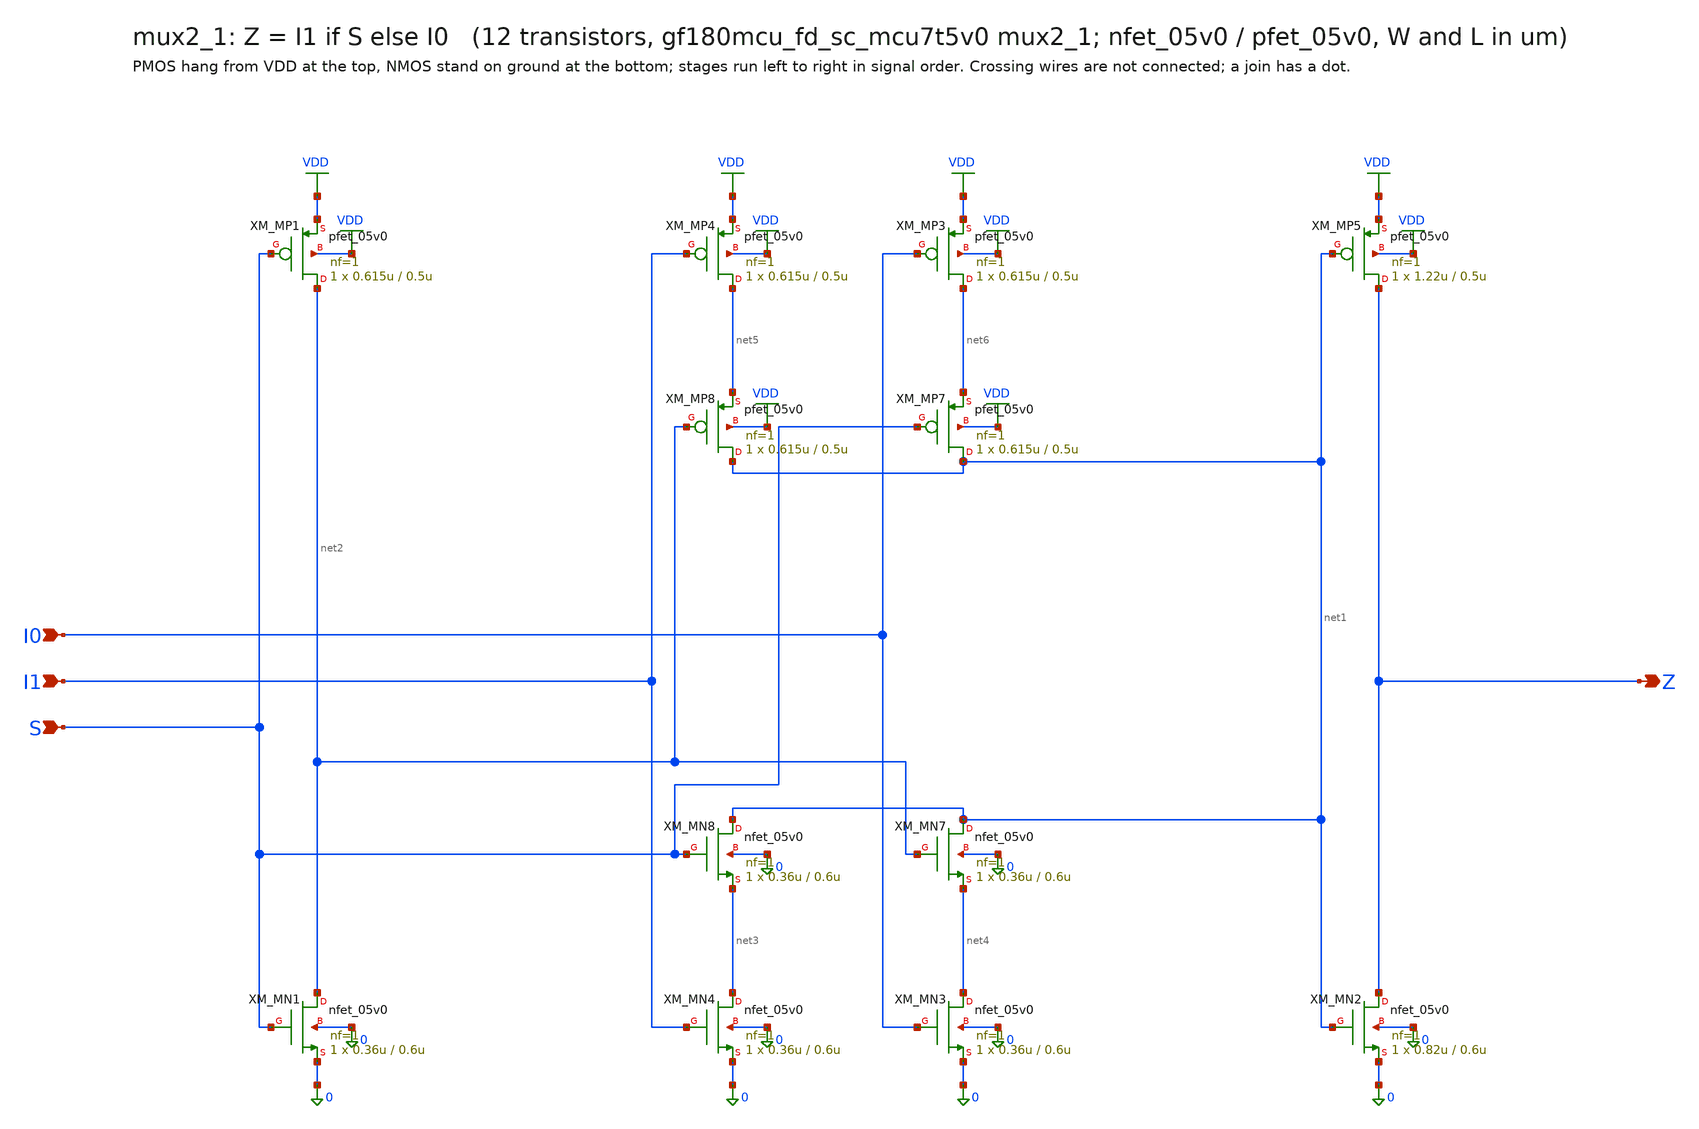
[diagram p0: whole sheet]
** sch_path: xschem/cells_tx/mux2_1.sch
**.subckt mux2_1 I0 I1 S Z
*.ipin I0
*.ipin I1
*.ipin S
*.opin Z
XM_MN2 Z net1 0 0 nfet_05v0 L=0.6u W=0.82u nf=1 ad=4.1e-13 as=4.1e-13 pd=2.64e-06 ps=2.64e-06 nrd=0
+ nrs=0 sa=0 sb=0 sd=0 m=1
XM_MN4 net3 I1 0 0 nfet_05v0 L=0.6u W=0.36u nf=1 ad=1.8e-13 as=1.8e-13 pd=1.72e-06 ps=1.72e-06 nrd=0
+ nrs=0 sa=0 sb=0 sd=0 m=1
XM_MN8 net1 S net3 0 nfet_05v0 L=0.6u W=0.36u nf=1 ad=1.8e-13 as=1.8e-13 pd=1.72e-06 ps=1.72e-06
+ nrd=0 nrs=0 sa=0 sb=0 sd=0 m=1
XM_MN7 net1 net2 net4 0 nfet_05v0 L=0.6u W=0.36u nf=1 ad=1.8e-13 as=1.8e-13 pd=1.72e-06 ps=1.72e-06
+ nrd=0 nrs=0 sa=0 sb=0 sd=0 m=1
XM_MN3 net4 I0 0 0 nfet_05v0 L=0.6u W=0.36u nf=1 ad=1.8e-13 as=1.8e-13 pd=1.72e-06 ps=1.72e-06 nrd=0
+ nrs=0 sa=0 sb=0 sd=0 m=1
XM_MN1 net2 S 0 0 nfet_05v0 L=0.6u W=0.36u nf=1 ad=1.8e-13 as=1.8e-13 pd=1.72e-06 ps=1.72e-06 nrd=0
+ nrs=0 sa=0 sb=0 sd=0 m=1
XM_MP5 Z net1 VDD VDD pfet_05v0 L=0.5u W=1.22u nf=1 ad=6.1e-13 as=6.1e-13 pd=3.44e-06 ps=3.44e-06
+ nrd=0 nrs=0 sa=0 sb=0 sd=0 m=1
XM_MP4 net5 I1 VDD VDD pfet_05v0 L=0.5u W=0.615u nf=1 ad=3.075e-13 as=3.075e-13 pd=2.23e-06
+ ps=2.23e-06 nrd=0 nrs=0 sa=0 sb=0 sd=0 m=1
XM_MP8 net1 net2 net5 VDD pfet_05v0 L=0.5u W=0.615u nf=1 ad=3.075e-13 as=3.075e-13 pd=2.23e-06
+ ps=2.23e-06 nrd=0 nrs=0 sa=0 sb=0 sd=0 m=1
XM_MP7 net1 S net6 VDD pfet_05v0 L=0.5u W=0.615u nf=1 ad=3.075e-13 as=3.075e-13 pd=2.23e-06
+ ps=2.23e-06 nrd=0 nrs=0 sa=0 sb=0 sd=0 m=1
XM_MP3 net6 I0 VDD VDD pfet_05v0 L=0.5u W=0.615u nf=1 ad=3.075e-13 as=3.075e-13 pd=2.23e-06
+ ps=2.23e-06 nrd=0 nrs=0 sa=0 sb=0 sd=0 m=1
XM_MP1 net2 S VDD VDD pfet_05v0 L=0.5u W=0.615u nf=1 ad=3.075e-13 as=3.075e-13 pd=2.23e-06
+ ps=2.23e-06 nrd=0 nrs=0 sa=0 sb=0 sd=0 m=1
**.ends
.GLOBAL VDD
.end
